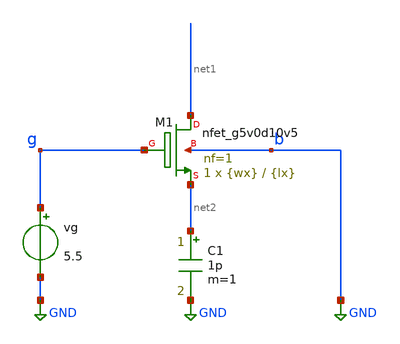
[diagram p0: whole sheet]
** sch_path: xschem/untitled-8.sch
**.subckt untitled-8
vg g GND 5.5
XM1 net1 g net2 GND sky130_fd_pr__nfet_g5v0d10v5 L={lx} W={wx} nf=1 ad='int((nf+1)/2) * W/nf * 0.29'
+ as='int((nf+2)/2) * W/nf * 0.29' pd='2*int((nf+1)/2) * (W/nf + 0.29)' ps='2*int((nf+2)/2) * (W/nf + 0.29)'
+ nrd='0.29 / W' nrs='0.29 / W' sa=0 sb=0 sd=0 mult=1 m=1
C1 net2 GND 1p m=1
**.ends
.GLOBAL GND
.end
